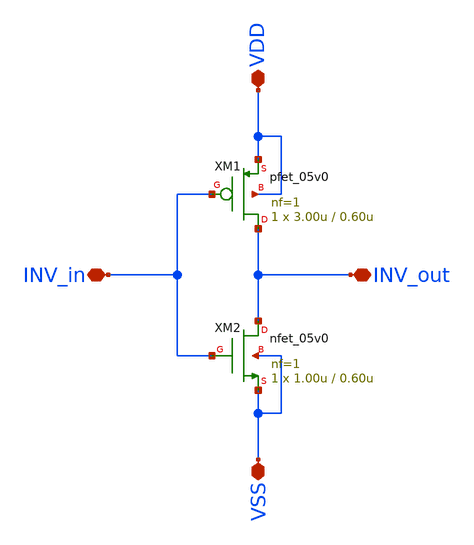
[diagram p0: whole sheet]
** sch_path: designs/libs/core_ldo/ldo/ldo_INV/INV.sch
**.subckt INV INV_in INV_out VDD VSS
*.iopin INV_in
*.iopin INV_out
*.iopin VDD
*.iopin VSS
XM1 INV_out INV_in VDD VDD pfet_05v0 L=0.60u W=3.00u nf=1 ad='int((nf+1)/2) * W/nf * 0.18u' as='int((nf+2)/2) * W/nf * 0.18u'
+ pd='2*int((nf+1)/2) * (W/nf + 0.18u)' ps='2*int((nf+2)/2) * (W/nf + 0.18u)' nrd='0.18u / W' nrs='0.18u / W'
+ sa=0 sb=0 sd=0 m=1
XM2 INV_out INV_in VSS VSS nfet_05v0 L=0.60u W=1.00u nf=1 ad='int((nf+1)/2) * W/nf * 0.18u' as='int((nf+2)/2) * W/nf * 0.18u'
+ pd='2*int((nf+1)/2) * (W/nf + 0.18u)' ps='2*int((nf+2)/2) * (W/nf + 0.18u)' nrd='0.18u / W' nrs='0.18u / W'
+ sa=0 sb=0 sd=0 m=1
**.ends
.end
